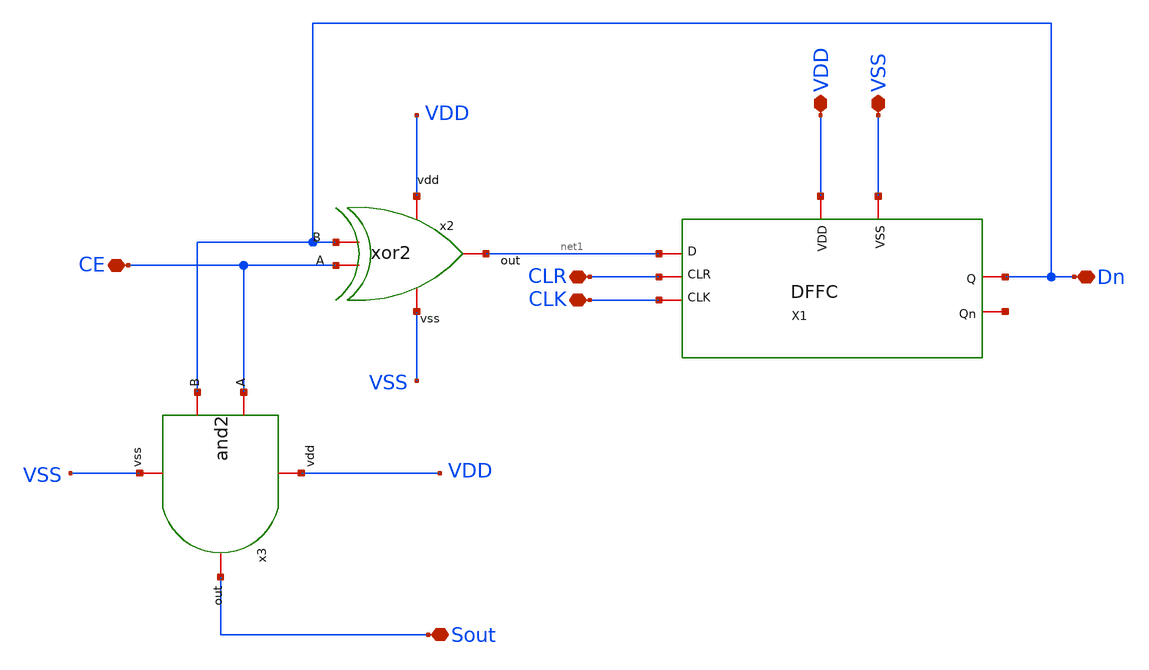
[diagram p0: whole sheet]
** sch_path: design/blocks/contador1bit_U/schematic/contador1bit_U.sch
**.subckt contador1bit_U CE CLR CLK VDD VSS Dn Sout
*.iopin CE
*.iopin CLR
*.iopin CLK
*.iopin VDD
*.iopin VSS
*.iopin Dn
*.iopin Sout
x2 VDD net1 Dn CE VSS xor2
x3 VDD CE Sout Dn VSS and2
x1 net1 VDD VSS Dn CLK CLR net2 dffc
**.ends
.end
